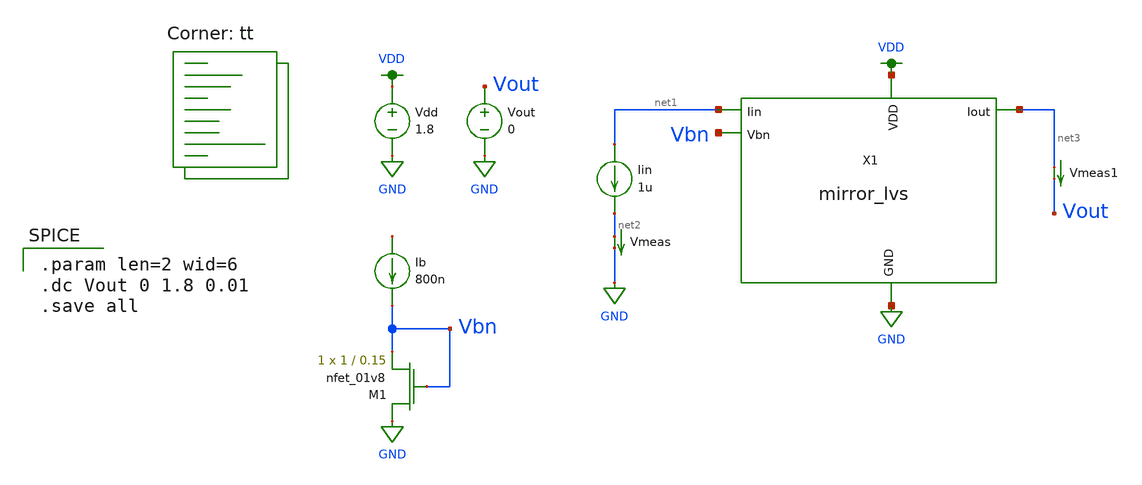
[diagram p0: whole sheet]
** sch_path: mp3/dac_tb.sch
**.subckt dac_tb
X1 net3 net1 GND Vbn VDD mirror_lvs
Vdd VDD GND 1.8
Vout Vout GND 0
Iin net1 net2 1u
Vmeas net2 GND 0
.save i(vmeas)
Ib net4 Vbn 800n
XM1 GND Vbn Vbn GND sky130_fd_pr__nfet_01v8 L=0.15 W=1 nf=1 ad='int((nf+1)/2) * W/nf * 0.29' as='int((nf+2)/2) * W/nf * 0.29'
+ pd='2*int((nf+1)/2) * (W/nf + 0.29)' ps='2*int((nf+2)/2) * (W/nf + 0.29)' nrd='0.29 / W' nrs='0.29 / W'
+ sa=0 sb=0 sd=0 mult=1 m=1
Vmeas1 net3 Vout 0
.save i(vmeas1)
**** begin user architecture code
.lib $::SKYWATER_MODELS/sky130.lib.spice tt

.param len=2 wid=6
.dc Vout 0 1.8 0.01
.save all


**** end user architecture code
**.ends

* expanding   symbol:  mirror_lvs.sym # of pins=5
** sym_path: mp3/mirror_lvs.sym
** sch_path: mp3/mirror_lvs.sch
.subckt mirror_lvs Iout Iin GND Vbn VDD
*.ipin Vbn
*.ipin Iin
*.iopin GND
*.iopin VDD
*.opin Iout
XM1 net3 net3 net4 VDD sky130_fd_pr__pfet_01v8 L={len} W={wid} nf=1 ad='int((nf+1)/2) * W/nf * 0.29'
+ as='int((nf+2)/2) * W/nf * 0.29' pd='2*int((nf+1)/2) * (W/nf + 0.29)' ps='2*int((nf+2)/2) * (W/nf + 0.29)'
+ nrd='0.29 / W' nrs='0.29 / W' sa=0 sb=0 sd=0 mult=1 m=1
XM2 net3 Vbn net2 GND sky130_fd_pr__nfet_01v8 L={len} W={wid} nf=1 ad='int((nf+1)/2) * W/nf * 0.29' as='int((nf+2)/2) * W/nf * 0.29'
+ pd='2*int((nf+1)/2) * (W/nf + 0.29)' ps='2*int((nf+2)/2) * (W/nf + 0.29)' nrd='0.29 / W' nrs='0.29 / W'
+ sa=0 sb=0 sd=0 mult=1 m=1
XM3 net2 Vbn net1 GND sky130_fd_pr__nfet_01v8 L={len} W={wid} nf=1 ad='int((nf+1)/2) * W/nf * 0.29' as='int((nf+2)/2) * W/nf * 0.29'
+ pd='2*int((nf+1)/2) * (W/nf + 0.29)' ps='2*int((nf+2)/2) * (W/nf + 0.29)' nrd='0.29 / W' nrs='0.29 / W'
+ sa=0 sb=0 sd=0 mult=1 m=1
XM4 net1 Vbn GND GND sky130_fd_pr__nfet_01v8 L={len} W={wid} nf=1 ad='int((nf+1)/2) * W/nf * 0.29' as='int((nf+2)/2) * W/nf * 0.29'
+ pd='2*int((nf+1)/2) * (W/nf + 0.29)' ps='2*int((nf+2)/2) * (W/nf + 0.29)' nrd='0.29 / W' nrs='0.29 / W'
+ sa=0 sb=0 sd=0 mult=1 m=1
XM5 GND Vbn net6 GND sky130_fd_pr__nfet_01v8 L={len} W={wid} nf=1 ad='int((nf+1)/2) * W/nf * 0.29' as='int((nf+2)/2) * W/nf * 0.29'
+ pd='2*int((nf+1)/2) * (W/nf + 0.29)' ps='2*int((nf+2)/2) * (W/nf + 0.29)' nrd='0.29 / W' nrs='0.29 / W'
+ sa=0 sb=0 sd=0 mult=1 m=1
XM6 net7 Vbn GND GND sky130_fd_pr__nfet_01v8 L={len} W={wid} nf=1 ad='int((nf+1)/2) * W/nf * 0.29' as='int((nf+2)/2) * W/nf * 0.29'
+ pd='2*int((nf+1)/2) * (W/nf + 0.29)' ps='2*int((nf+2)/2) * (W/nf + 0.29)' nrd='0.29 / W' nrs='0.29 / W'
+ sa=0 sb=0 sd=0 mult=1 m=1
XM7 GND Vbn net8 GND sky130_fd_pr__nfet_01v8 L={len} W={wid} nf=1 ad='int((nf+1)/2) * W/nf * 0.29' as='int((nf+2)/2) * W/nf * 0.29'
+ pd='2*int((nf+1)/2) * (W/nf + 0.29)' ps='2*int((nf+2)/2) * (W/nf + 0.29)' nrd='0.29 / W' nrs='0.29 / W'
+ sa=0 sb=0 sd=0 mult=1 m=1
XM8 net4 net3 VDD VDD sky130_fd_pr__pfet_01v8 L={len} W={wid} nf=1 ad='int((nf+1)/2) * W/nf * 0.29' as='int((nf+2)/2) * W/nf * 0.29'
+ pd='2*int((nf+1)/2) * (W/nf + 0.29)' ps='2*int((nf+2)/2) * (W/nf + 0.29)' nrd='0.29 / W' nrs='0.29 / W'
+ sa=0 sb=0 sd=0 mult=1 m=1
XM9 net4 net3 net3 VDD sky130_fd_pr__pfet_01v8 L={len} W={wid} nf=1 ad='int((nf+1)/2) * W/nf * 0.29'
+ as='int((nf+2)/2) * W/nf * 0.29' pd='2*int((nf+1)/2) * (W/nf + 0.29)' ps='2*int((nf+2)/2) * (W/nf + 0.29)'
+ nrd='0.29 / W' nrs='0.29 / W' sa=0 sb=0 sd=0 mult=1 m=1
XM10 net6 net6 net4 VDD sky130_fd_pr__pfet_01v8 L={len} W={wid} nf=1 ad='int((nf+1)/2) * W/nf * 0.29'
+ as='int((nf+2)/2) * W/nf * 0.29' pd='2*int((nf+1)/2) * (W/nf + 0.29)' ps='2*int((nf+2)/2) * (W/nf + 0.29)'
+ nrd='0.29 / W' nrs='0.29 / W' sa=0 sb=0 sd=0 mult=1 m=1
XM11 Iin net8 VDD VDD sky130_fd_pr__pfet_01v8 L={len} W={wid} nf=1 ad='int((nf+1)/2) * W/nf * 0.29' as='int((nf+2)/2) * W/nf * 0.29'
+ pd='2*int((nf+1)/2) * (W/nf + 0.29)' ps='2*int((nf+2)/2) * (W/nf + 0.29)' nrd='0.29 / W' nrs='0.29 / W'
+ sa=0 sb=0 sd=0 mult=1 m=1
XM12 Iin net6 net7 VDD sky130_fd_pr__pfet_01v8 L={len} W={wid} nf=1 ad='int((nf+1)/2) * W/nf * 0.29'
+ as='int((nf+2)/2) * W/nf * 0.29' pd='2*int((nf+1)/2) * (W/nf + 0.29)' ps='2*int((nf+2)/2) * (W/nf + 0.29)'
+ nrd='0.29 / W' nrs='0.29 / W' sa=0 sb=0 sd=0 mult=1 m=1
XM13 VDD net8 net5 VDD sky130_fd_pr__pfet_01v8 L={len} W={wid} nf=1 ad='int((nf+1)/2) * W/nf * 0.29'
+ as='int((nf+2)/2) * W/nf * 0.29' pd='2*int((nf+1)/2) * (W/nf + 0.29)' ps='2*int((nf+2)/2) * (W/nf + 0.29)'
+ nrd='0.29 / W' nrs='0.29 / W' sa=0 sb=0 sd=0 mult=1 m=1
XM14 net8 net6 net5 VDD sky130_fd_pr__pfet_01v8 L={len} W={wid} nf=1 ad='int((nf+1)/2) * W/nf * 0.29'
+ as='int((nf+2)/2) * W/nf * 0.29' pd='2*int((nf+1)/2) * (W/nf + 0.29)' ps='2*int((nf+2)/2) * (W/nf + 0.29)'
+ nrd='0.29 / W' nrs='0.29 / W' sa=0 sb=0 sd=0 mult=1 m=1
XM15 net5 net7 Iout VDD sky130_fd_pr__pfet_01v8 L={len} W={wid} nf=1 ad='int((nf+1)/2) * W/nf * 0.29'
+ as='int((nf+2)/2) * W/nf * 0.29' pd='2*int((nf+1)/2) * (W/nf + 0.29)' ps='2*int((nf+2)/2) * (W/nf + 0.29)'
+ nrd='0.29 / W' nrs='0.29 / W' sa=0 sb=0 sd=0 mult=1 m=1
XM16 net11 net11 net12 VDD sky130_fd_pr__pfet_01v8 L={len} W={wid} nf=1 ad='int((nf+1)/2) * W/nf * 0.29'
+ as='int((nf+2)/2) * W/nf * 0.29' pd='2*int((nf+1)/2) * (W/nf + 0.29)' ps='2*int((nf+2)/2) * (W/nf + 0.29)'
+ nrd='0.29 / W' nrs='0.29 / W' sa=0 sb=0 sd=0 mult=1 m=1
XM17 net11 Vbn net10 GND sky130_fd_pr__nfet_01v8 L={len} W={wid} nf=1 ad='int((nf+1)/2) * W/nf * 0.29'
+ as='int((nf+2)/2) * W/nf * 0.29' pd='2*int((nf+1)/2) * (W/nf + 0.29)' ps='2*int((nf+2)/2) * (W/nf + 0.29)'
+ nrd='0.29 / W' nrs='0.29 / W' sa=0 sb=0 sd=0 mult=1 m=1
XM18 net10 Vbn net9 GND sky130_fd_pr__nfet_01v8 L={len} W={wid} nf=1 ad='int((nf+1)/2) * W/nf * 0.29'
+ as='int((nf+2)/2) * W/nf * 0.29' pd='2*int((nf+1)/2) * (W/nf + 0.29)' ps='2*int((nf+2)/2) * (W/nf + 0.29)'
+ nrd='0.29 / W' nrs='0.29 / W' sa=0 sb=0 sd=0 mult=1 m=1
XM19 net9 Vbn GND GND sky130_fd_pr__nfet_01v8 L={len} W={wid} nf=1 ad='int((nf+1)/2) * W/nf * 0.29' as='int((nf+2)/2) * W/nf * 0.29'
+ pd='2*int((nf+1)/2) * (W/nf + 0.29)' ps='2*int((nf+2)/2) * (W/nf + 0.29)' nrd='0.29 / W' nrs='0.29 / W'
+ sa=0 sb=0 sd=0 mult=1 m=1
XM20 GND Vbn net14 GND sky130_fd_pr__nfet_01v8 L={len} W={wid} nf=1 ad='int((nf+1)/2) * W/nf * 0.29'
+ as='int((nf+2)/2) * W/nf * 0.29' pd='2*int((nf+1)/2) * (W/nf + 0.29)' ps='2*int((nf+2)/2) * (W/nf + 0.29)'
+ nrd='0.29 / W' nrs='0.29 / W' sa=0 sb=0 sd=0 mult=1 m=1
XM21 net15 Vbn GND GND sky130_fd_pr__nfet_01v8 L={len} W={wid} nf=1 ad='int((nf+1)/2) * W/nf * 0.29'
+ as='int((nf+2)/2) * W/nf * 0.29' pd='2*int((nf+1)/2) * (W/nf + 0.29)' ps='2*int((nf+2)/2) * (W/nf + 0.29)'
+ nrd='0.29 / W' nrs='0.29 / W' sa=0 sb=0 sd=0 mult=1 m=1
XM22 GND Vbn net16 GND sky130_fd_pr__nfet_01v8 L={len} W={wid} nf=1 ad='int((nf+1)/2) * W/nf * 0.29'
+ as='int((nf+2)/2) * W/nf * 0.29' pd='2*int((nf+1)/2) * (W/nf + 0.29)' ps='2*int((nf+2)/2) * (W/nf + 0.29)'
+ nrd='0.29 / W' nrs='0.29 / W' sa=0 sb=0 sd=0 mult=1 m=1
XM23 net12 net11 VDD VDD sky130_fd_pr__pfet_01v8 L={len} W={wid} nf=1 ad='int((nf+1)/2) * W/nf * 0.29'
+ as='int((nf+2)/2) * W/nf * 0.29' pd='2*int((nf+1)/2) * (W/nf + 0.29)' ps='2*int((nf+2)/2) * (W/nf + 0.29)'
+ nrd='0.29 / W' nrs='0.29 / W' sa=0 sb=0 sd=0 mult=1 m=1
XM24 net12 net11 net11 VDD sky130_fd_pr__pfet_01v8 L={len} W={wid} nf=1 ad='int((nf+1)/2) * W/nf * 0.29'
+ as='int((nf+2)/2) * W/nf * 0.29' pd='2*int((nf+1)/2) * (W/nf + 0.29)' ps='2*int((nf+2)/2) * (W/nf + 0.29)'
+ nrd='0.29 / W' nrs='0.29 / W' sa=0 sb=0 sd=0 mult=1 m=1
XM25 net14 net14 net12 VDD sky130_fd_pr__pfet_01v8 L={len} W={wid} nf=1 ad='int((nf+1)/2) * W/nf * 0.29'
+ as='int((nf+2)/2) * W/nf * 0.29' pd='2*int((nf+1)/2) * (W/nf + 0.29)' ps='2*int((nf+2)/2) * (W/nf + 0.29)'
+ nrd='0.29 / W' nrs='0.29 / W' sa=0 sb=0 sd=0 mult=1 m=1
XM26 Iin net16 VDD VDD sky130_fd_pr__pfet_01v8 L={len} W={wid} nf=1 ad='int((nf+1)/2) * W/nf * 0.29'
+ as='int((nf+2)/2) * W/nf * 0.29' pd='2*int((nf+1)/2) * (W/nf + 0.29)' ps='2*int((nf+2)/2) * (W/nf + 0.29)'
+ nrd='0.29 / W' nrs='0.29 / W' sa=0 sb=0 sd=0 mult=1 m=1
XM27 Iin net14 net15 VDD sky130_fd_pr__pfet_01v8 L={len} W={wid} nf=1 ad='int((nf+1)/2) * W/nf * 0.29'
+ as='int((nf+2)/2) * W/nf * 0.29' pd='2*int((nf+1)/2) * (W/nf + 0.29)' ps='2*int((nf+2)/2) * (W/nf + 0.29)'
+ nrd='0.29 / W' nrs='0.29 / W' sa=0 sb=0 sd=0 mult=1 m=1
XM28 VDD net16 net13 VDD sky130_fd_pr__pfet_01v8 L={len} W={wid} nf=1 ad='int((nf+1)/2) * W/nf * 0.29'
+ as='int((nf+2)/2) * W/nf * 0.29' pd='2*int((nf+1)/2) * (W/nf + 0.29)' ps='2*int((nf+2)/2) * (W/nf + 0.29)'
+ nrd='0.29 / W' nrs='0.29 / W' sa=0 sb=0 sd=0 mult=1 m=1
XM29 net16 net14 net13 VDD sky130_fd_pr__pfet_01v8 L={len} W={wid} nf=1 ad='int((nf+1)/2) * W/nf * 0.29'
+ as='int((nf+2)/2) * W/nf * 0.29' pd='2*int((nf+1)/2) * (W/nf + 0.29)' ps='2*int((nf+2)/2) * (W/nf + 0.29)'
+ nrd='0.29 / W' nrs='0.29 / W' sa=0 sb=0 sd=0 mult=1 m=1
XM30 net13 net15 Iout VDD sky130_fd_pr__pfet_01v8 L={len} W={wid} nf=1 ad='int((nf+1)/2) * W/nf * 0.29'
+ as='int((nf+2)/2) * W/nf * 0.29' pd='2*int((nf+1)/2) * (W/nf + 0.29)' ps='2*int((nf+2)/2) * (W/nf + 0.29)'
+ nrd='0.29 / W' nrs='0.29 / W' sa=0 sb=0 sd=0 mult=1 m=1
.ends

.GLOBAL VDD
.GLOBAL GND
.end
